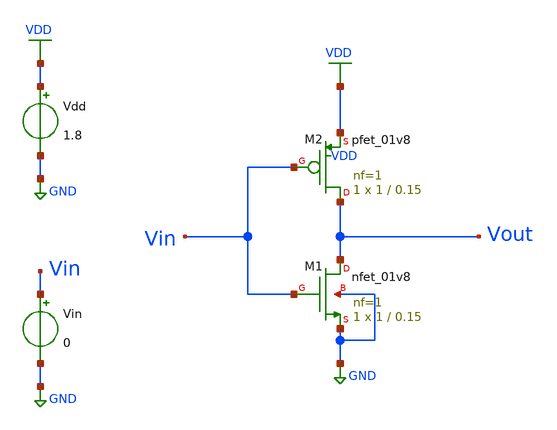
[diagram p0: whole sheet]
** sch_path: projects/inverter_tutorial/xschem_ngspice/inverter_vtc.sch
**.subckt inverter_vtc
XM1 Vout Vin GND GND sky130_fd_pr__nfet_01v8 L=0.15 W=1 nf=1 ad='int((nf+1)/2) * W/nf * 0.29' as='int((nf+2)/2) * W/nf * 0.29'
+ pd='2*int((nf+1)/2) * (W/nf + 0.29)' ps='2*int((nf+2)/2) * (W/nf + 0.29)' nrd='0.29 / W' nrs='0.29 / W'
+ sa=0 sb=0 sd=0 mult=1 m=1
XM2 Vout Vin VDD VDD sky130_fd_pr__pfet_01v8 L=0.15 W=1 nf=1 ad='int((nf+1)/2) * W/nf * 0.29' as='int((nf+2)/2) * W/nf * 0.29'
+ pd='2*int((nf+1)/2) * (W/nf + 0.29)' ps='2*int((nf+2)/2) * (W/nf + 0.29)' nrd='0.29 / W' nrs='0.29 / W'
+ sa=0 sb=0 sd=0 mult=1 m=1
Vin Vin GND 0
Vdd VDD GND 1.8
**** begin user architecture code



.lib /foss/pdks/sky130A/libs.tech/ngspice/sky130.lib.spice tt

.dc Vin 0 1.8 0.01
.save all



**** end user architecture code
**.ends
.GLOBAL VDD
.GLOBAL GND
.end
